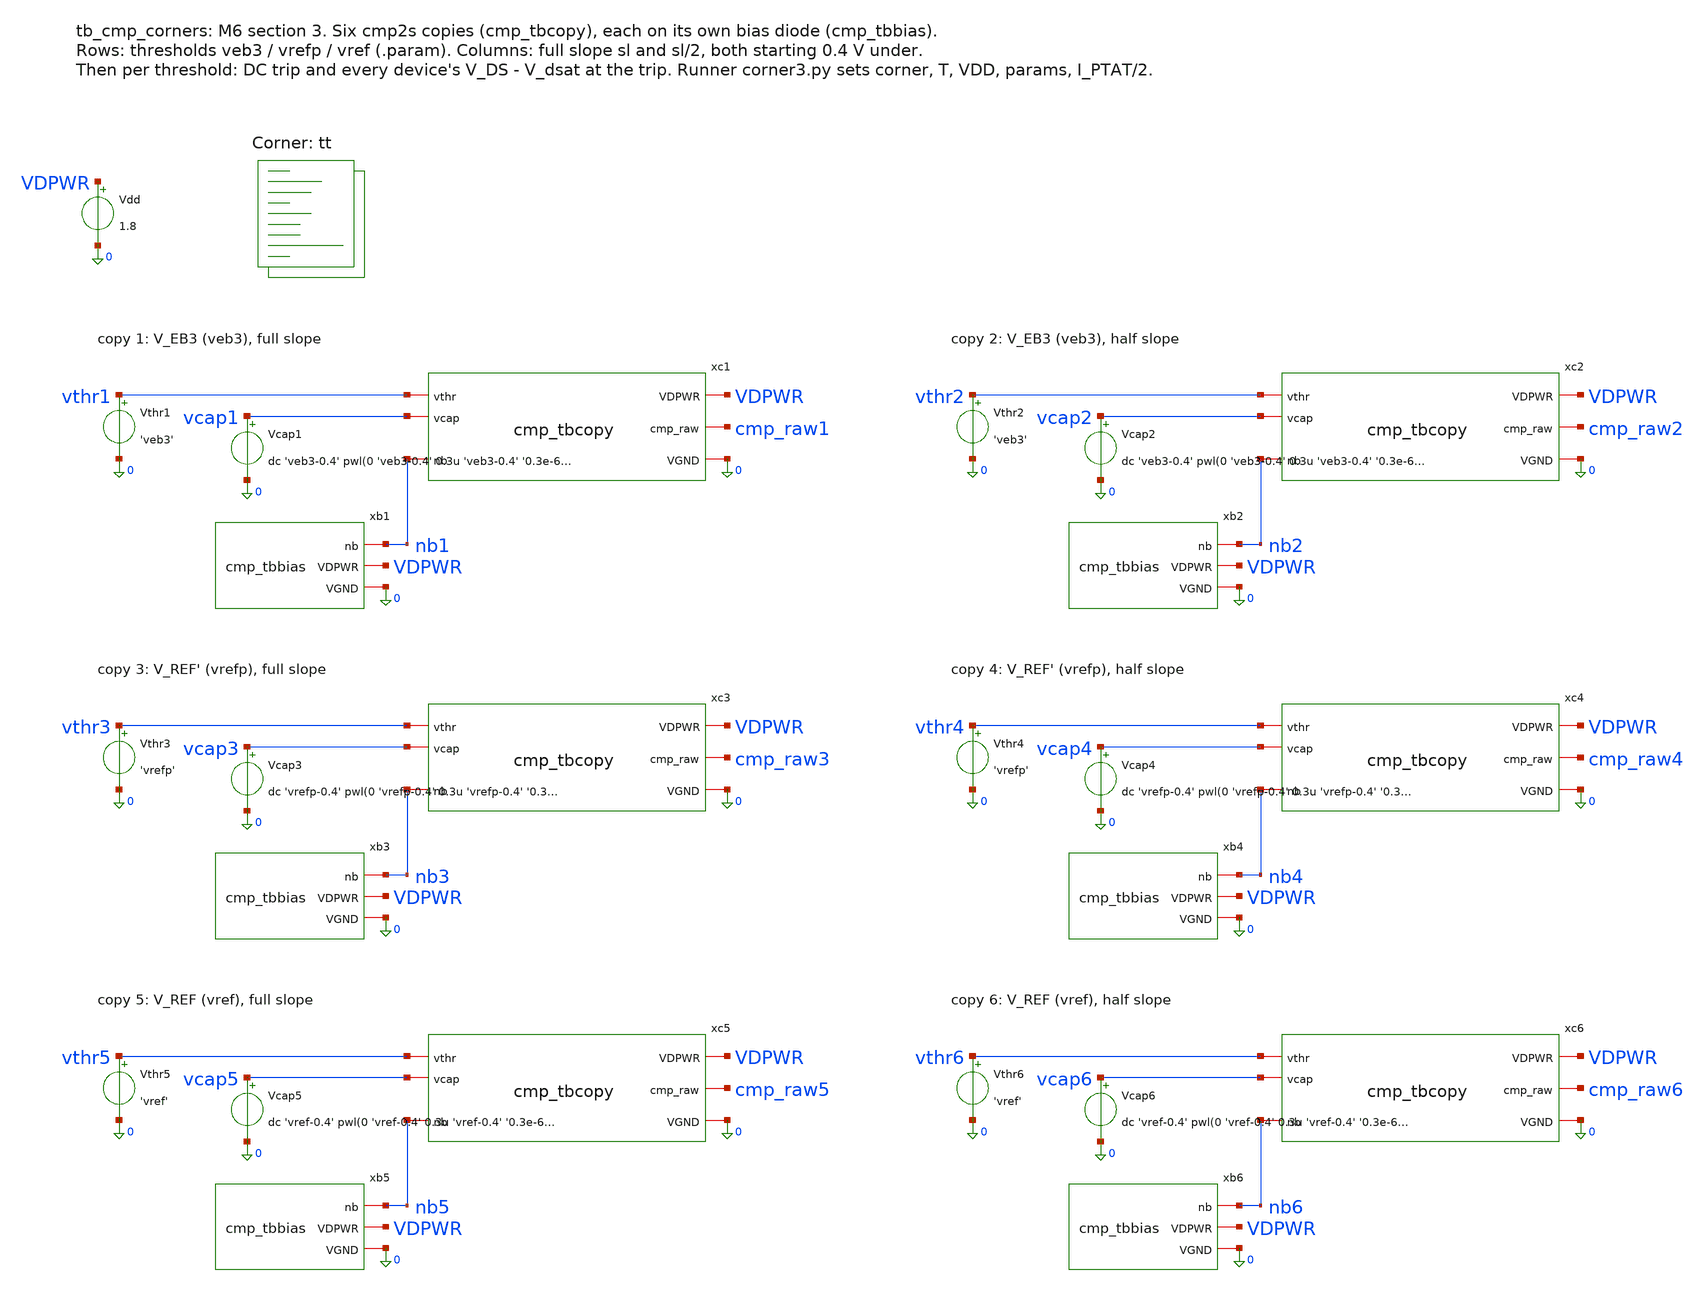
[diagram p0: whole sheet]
** sch_path: xschem/tb_cmp_corners.sch
**.subckt tb_cmp_corners
xc1 vthr1 vcap1 nb1 VDPWR cmp_raw1 0 cmp_tbcopy
xb1 nb1 VDPWR 0 cmp_tbbias
Vthr1 vthr1 0 'veb3'
Vcap1 vcap1 0 dc 'veb3-0.4' pwl(0 'veb3-0.4' 0.3u 'veb3-0.4' '0.3e-6+0.46/sl' 'veb3+0.06')
xc2 vthr2 vcap2 nb2 VDPWR cmp_raw2 0 cmp_tbcopy
xb2 nb2 VDPWR 0 cmp_tbbias
Vthr2 vthr2 0 'veb3'
Vcap2 vcap2 0 dc 'veb3-0.4' pwl(0 'veb3-0.4' 0.3u 'veb3-0.4' '0.3e-6+0.92/sl' 'veb3+0.06')
xc3 vthr3 vcap3 nb3 VDPWR cmp_raw3 0 cmp_tbcopy
xb3 nb3 VDPWR 0 cmp_tbbias
Vthr3 vthr3 0 'vrefp'
Vcap3 vcap3 0 dc 'vrefp-0.4' pwl(0 'vrefp-0.4' 0.3u 'vrefp-0.4' '0.3e-6+0.46/sl' 'vrefp+0.06')
xc4 vthr4 vcap4 nb4 VDPWR cmp_raw4 0 cmp_tbcopy
xb4 nb4 VDPWR 0 cmp_tbbias
Vthr4 vthr4 0 'vrefp'
Vcap4 vcap4 0 dc 'vrefp-0.4' pwl(0 'vrefp-0.4' 0.3u 'vrefp-0.4' '0.3e-6+0.92/sl' 'vrefp+0.06')
xc5 vthr5 vcap5 nb5 VDPWR cmp_raw5 0 cmp_tbcopy
xb5 nb5 VDPWR 0 cmp_tbbias
Vthr5 vthr5 0 'vref'
Vcap5 vcap5 0 dc 'vref-0.4' pwl(0 'vref-0.4' 0.3u 'vref-0.4' '0.3e-6+0.46/sl' 'vref+0.06')
xc6 vthr6 vcap6 nb6 VDPWR cmp_raw6 0 cmp_tbcopy
xb6 nb6 VDPWR 0 cmp_tbbias
Vthr6 vthr6 0 'vref'
Vcap6 vcap6 0 dc 'vref-0.4' pwl(0 'vref-0.4' 0.3u 'vref-0.4' '0.3e-6+0.92/sl' 'vref+0.06')
Vdd VDPWR 0 1.8
**** begin user architecture code

.param vref=1.2432 veb3=0.7096 vrefp=0.9605 sl=0.274e6
.include /foss/pdks/sky130A/libs.ref/sky130_fd_sc_hd/spice/sky130_fd_sc_hd.spice
.option method=gear
.temp 25
.control
save all @m.xc1.x1.xm1a.msky130_fd_pr__nfet_01v8_lvt[vds]
+ @m.xc1.x1.xm1a.msky130_fd_pr__nfet_01v8_lvt[vdsat] @m.xc1.x1.xm1b.msky130_fd_pr__nfet_01v8_lvt[vds] @m.xc1.x1.xm1b.msky130_fd_pr__nfet_01v8_lvt[vdsat]
+ @m.xc1.x1.xm2b.msky130_fd_pr__pfet_01v8_lvt[vds] @m.xc1.x1.xm2b.msky130_fd_pr__pfet_01v8_lvt[vdsat] @m.xc1.x1.xm3.msky130_fd_pr__pfet_01v8_lvt[vds]
+ @m.xc1.x1.xm3.msky130_fd_pr__pfet_01v8_lvt[vdsat] @m.xc1.xmnb3.msky130_fd_pr__nfet_01v8[vds] @m.xc1.xmnb3.msky130_fd_pr__nfet_01v8[vdsat]
+ @m.xc2.x1.xm1a.msky130_fd_pr__nfet_01v8_lvt[vds] @m.xc2.x1.xm1a.msky130_fd_pr__nfet_01v8_lvt[vdsat] @m.xc2.x1.xm1b.msky130_fd_pr__nfet_01v8_lvt[vds]
+ @m.xc2.x1.xm1b.msky130_fd_pr__nfet_01v8_lvt[vdsat] @m.xc2.x1.xm2b.msky130_fd_pr__pfet_01v8_lvt[vds] @m.xc2.x1.xm2b.msky130_fd_pr__pfet_01v8_lvt[vdsat]
+ @m.xc2.x1.xm3.msky130_fd_pr__pfet_01v8_lvt[vds] @m.xc2.x1.xm3.msky130_fd_pr__pfet_01v8_lvt[vdsat] @m.xc2.xmnb3.msky130_fd_pr__nfet_01v8[vds]
+ @m.xc2.xmnb3.msky130_fd_pr__nfet_01v8[vdsat] @m.xc3.x1.xm1a.msky130_fd_pr__nfet_01v8_lvt[vds] @m.xc3.x1.xm1a.msky130_fd_pr__nfet_01v8_lvt[vdsat]
+ @m.xc3.x1.xm1b.msky130_fd_pr__nfet_01v8_lvt[vds] @m.xc3.x1.xm1b.msky130_fd_pr__nfet_01v8_lvt[vdsat] @m.xc3.x1.xm2b.msky130_fd_pr__pfet_01v8_lvt[vds]
+ @m.xc3.x1.xm2b.msky130_fd_pr__pfet_01v8_lvt[vdsat] @m.xc3.x1.xm3.msky130_fd_pr__pfet_01v8_lvt[vds] @m.xc3.x1.xm3.msky130_fd_pr__pfet_01v8_lvt[vdsat]
+ @m.xc3.xmnb3.msky130_fd_pr__nfet_01v8[vds] @m.xc3.xmnb3.msky130_fd_pr__nfet_01v8[vdsat] @m.xc4.x1.xm1a.msky130_fd_pr__nfet_01v8_lvt[vds]
+ @m.xc4.x1.xm1a.msky130_fd_pr__nfet_01v8_lvt[vdsat] @m.xc4.x1.xm1b.msky130_fd_pr__nfet_01v8_lvt[vds] @m.xc4.x1.xm1b.msky130_fd_pr__nfet_01v8_lvt[vdsat]
+ @m.xc4.x1.xm2b.msky130_fd_pr__pfet_01v8_lvt[vds] @m.xc4.x1.xm2b.msky130_fd_pr__pfet_01v8_lvt[vdsat] @m.xc4.x1.xm3.msky130_fd_pr__pfet_01v8_lvt[vds]
+ @m.xc4.x1.xm3.msky130_fd_pr__pfet_01v8_lvt[vdsat] @m.xc4.xmnb3.msky130_fd_pr__nfet_01v8[vds] @m.xc4.xmnb3.msky130_fd_pr__nfet_01v8[vdsat]
+ @m.xc5.x1.xm1a.msky130_fd_pr__nfet_01v8_lvt[vds] @m.xc5.x1.xm1a.msky130_fd_pr__nfet_01v8_lvt[vdsat] @m.xc5.x1.xm1b.msky130_fd_pr__nfet_01v8_lvt[vds]
+ @m.xc5.x1.xm1b.msky130_fd_pr__nfet_01v8_lvt[vdsat] @m.xc5.x1.xm2b.msky130_fd_pr__pfet_01v8_lvt[vds] @m.xc5.x1.xm2b.msky130_fd_pr__pfet_01v8_lvt[vdsat]
+ @m.xc5.x1.xm3.msky130_fd_pr__pfet_01v8_lvt[vds] @m.xc5.x1.xm3.msky130_fd_pr__pfet_01v8_lvt[vdsat] @m.xc5.xmnb3.msky130_fd_pr__nfet_01v8[vds]
+ @m.xc5.xmnb3.msky130_fd_pr__nfet_01v8[vdsat] @m.xc6.x1.xm1a.msky130_fd_pr__nfet_01v8_lvt[vds] @m.xc6.x1.xm1a.msky130_fd_pr__nfet_01v8_lvt[vdsat]
+ @m.xc6.x1.xm1b.msky130_fd_pr__nfet_01v8_lvt[vds] @m.xc6.x1.xm1b.msky130_fd_pr__nfet_01v8_lvt[vdsat] @m.xc6.x1.xm2b.msky130_fd_pr__pfet_01v8_lvt[vds]
+ @m.xc6.x1.xm2b.msky130_fd_pr__pfet_01v8_lvt[vdsat] @m.xc6.x1.xm3.msky130_fd_pr__pfet_01v8_lvt[vds] @m.xc6.x1.xm3.msky130_fd_pr__pfet_01v8_lvt[vdsat]
+ @m.xc6.xmnb3.msky130_fd_pr__nfet_01v8[vds] @m.xc6.xmnb3.msky130_fd_pr__nfet_01v8[vdsat]
tran 0.2n 3.85u 0 0.2n
meas tran to1 when v(cmp_raw1)=0.9 rise=1
meas tran to2 when v(cmp_raw2)=0.9 rise=1
meas tran to3 when v(cmp_raw3)=0.9 rise=1
meas tran to4 when v(cmp_raw4)=0.9 rise=1
meas tran to5 when v(cmp_raw5)=0.9 rise=1
meas tran to6 when v(cmp_raw6)=0.9 rise=1
echo RESULT to1=$&to1 to2=$&to2 to3=$&to3 to4=$&to4 to5=$&to5 to6=$&to6
* V_DS - V_dsat (mV) of the key devices at the moment n2 crosses 0.9 V on the ramp
meas tran tf1 when v(xc1.ib_cmp2)=0.9 rise=1
let gm1a_1 = (abs(@m.xc1.x1.xm1a.msky130_fd_pr__nfet_01v8_lvt[vds]) -
+ abs(@m.xc1.x1.xm1a.msky130_fd_pr__nfet_01v8_lvt[vdsat]))*1e3
meas tran fm1a_1 find gm1a_1 at=$&tf1
let gm1b_1 = (abs(@m.xc1.x1.xm1b.msky130_fd_pr__nfet_01v8_lvt[vds]) -
+ abs(@m.xc1.x1.xm1b.msky130_fd_pr__nfet_01v8_lvt[vdsat]))*1e3
meas tran fm1b_1 find gm1b_1 at=$&tf1
let gm2b_1 = (abs(@m.xc1.x1.xm2b.msky130_fd_pr__pfet_01v8_lvt[vds]) -
+ abs(@m.xc1.x1.xm2b.msky130_fd_pr__pfet_01v8_lvt[vdsat]))*1e3
meas tran fm2b_1 find gm2b_1 at=$&tf1
let gm3_1 = (abs(@m.xc1.x1.xm3.msky130_fd_pr__pfet_01v8_lvt[vds]) -
+ abs(@m.xc1.x1.xm3.msky130_fd_pr__pfet_01v8_lvt[vdsat]))*1e3
meas tran fm3_1 find gm3_1 at=$&tf1
let gmnb3_1 = (abs(@m.xc1.xmnb3.msky130_fd_pr__nfet_01v8[vds]) -
+ abs(@m.xc1.xmnb3.msky130_fd_pr__nfet_01v8[vdsat]))*1e3
meas tran fmnb3_1 find gmnb3_1 at=$&tf1
meas tran fn1_1 find v(xc1.x1.n1) at=$&tf1
meas tran ftl_1 find v(xc1.ib_cmp1) at=$&tf1
echo FLIP k=1 m1a=$&fm1a_1 m1b=$&fm1b_1 m2b=$&fm2b_1 m3=$&fm3_1 mnb3=$&fmnb3_1 n1=$&fn1_1
+ tail=$&ftl_1
meas tran tf2 when v(xc2.ib_cmp2)=0.9 rise=1
let gm1a_2 = (abs(@m.xc2.x1.xm1a.msky130_fd_pr__nfet_01v8_lvt[vds]) -
+ abs(@m.xc2.x1.xm1a.msky130_fd_pr__nfet_01v8_lvt[vdsat]))*1e3
meas tran fm1a_2 find gm1a_2 at=$&tf2
let gm1b_2 = (abs(@m.xc2.x1.xm1b.msky130_fd_pr__nfet_01v8_lvt[vds]) -
+ abs(@m.xc2.x1.xm1b.msky130_fd_pr__nfet_01v8_lvt[vdsat]))*1e3
meas tran fm1b_2 find gm1b_2 at=$&tf2
let gm2b_2 = (abs(@m.xc2.x1.xm2b.msky130_fd_pr__pfet_01v8_lvt[vds]) -
+ abs(@m.xc2.x1.xm2b.msky130_fd_pr__pfet_01v8_lvt[vdsat]))*1e3
meas tran fm2b_2 find gm2b_2 at=$&tf2
let gm3_2 = (abs(@m.xc2.x1.xm3.msky130_fd_pr__pfet_01v8_lvt[vds]) -
+ abs(@m.xc2.x1.xm3.msky130_fd_pr__pfet_01v8_lvt[vdsat]))*1e3
meas tran fm3_2 find gm3_2 at=$&tf2
let gmnb3_2 = (abs(@m.xc2.xmnb3.msky130_fd_pr__nfet_01v8[vds]) -
+ abs(@m.xc2.xmnb3.msky130_fd_pr__nfet_01v8[vdsat]))*1e3
meas tran fmnb3_2 find gmnb3_2 at=$&tf2
meas tran fn1_2 find v(xc2.x1.n1) at=$&tf2
meas tran ftl_2 find v(xc2.ib_cmp1) at=$&tf2
echo FLIP k=2 m1a=$&fm1a_2 m1b=$&fm1b_2 m2b=$&fm2b_2 m3=$&fm3_2 mnb3=$&fmnb3_2 n1=$&fn1_2
+ tail=$&ftl_2
meas tran tf3 when v(xc3.ib_cmp2)=0.9 rise=1
let gm1a_3 = (abs(@m.xc3.x1.xm1a.msky130_fd_pr__nfet_01v8_lvt[vds]) -
+ abs(@m.xc3.x1.xm1a.msky130_fd_pr__nfet_01v8_lvt[vdsat]))*1e3
meas tran fm1a_3 find gm1a_3 at=$&tf3
let gm1b_3 = (abs(@m.xc3.x1.xm1b.msky130_fd_pr__nfet_01v8_lvt[vds]) -
+ abs(@m.xc3.x1.xm1b.msky130_fd_pr__nfet_01v8_lvt[vdsat]))*1e3
meas tran fm1b_3 find gm1b_3 at=$&tf3
let gm2b_3 = (abs(@m.xc3.x1.xm2b.msky130_fd_pr__pfet_01v8_lvt[vds]) -
+ abs(@m.xc3.x1.xm2b.msky130_fd_pr__pfet_01v8_lvt[vdsat]))*1e3
meas tran fm2b_3 find gm2b_3 at=$&tf3
let gm3_3 = (abs(@m.xc3.x1.xm3.msky130_fd_pr__pfet_01v8_lvt[vds]) -
+ abs(@m.xc3.x1.xm3.msky130_fd_pr__pfet_01v8_lvt[vdsat]))*1e3
meas tran fm3_3 find gm3_3 at=$&tf3
let gmnb3_3 = (abs(@m.xc3.xmnb3.msky130_fd_pr__nfet_01v8[vds]) -
+ abs(@m.xc3.xmnb3.msky130_fd_pr__nfet_01v8[vdsat]))*1e3
meas tran fmnb3_3 find gmnb3_3 at=$&tf3
meas tran fn1_3 find v(xc3.x1.n1) at=$&tf3
meas tran ftl_3 find v(xc3.ib_cmp1) at=$&tf3
echo FLIP k=3 m1a=$&fm1a_3 m1b=$&fm1b_3 m2b=$&fm2b_3 m3=$&fm3_3 mnb3=$&fmnb3_3 n1=$&fn1_3
+ tail=$&ftl_3
meas tran tf4 when v(xc4.ib_cmp2)=0.9 rise=1
let gm1a_4 = (abs(@m.xc4.x1.xm1a.msky130_fd_pr__nfet_01v8_lvt[vds]) -
+ abs(@m.xc4.x1.xm1a.msky130_fd_pr__nfet_01v8_lvt[vdsat]))*1e3
meas tran fm1a_4 find gm1a_4 at=$&tf4
let gm1b_4 = (abs(@m.xc4.x1.xm1b.msky130_fd_pr__nfet_01v8_lvt[vds]) -
+ abs(@m.xc4.x1.xm1b.msky130_fd_pr__nfet_01v8_lvt[vdsat]))*1e3
meas tran fm1b_4 find gm1b_4 at=$&tf4
let gm2b_4 = (abs(@m.xc4.x1.xm2b.msky130_fd_pr__pfet_01v8_lvt[vds]) -
+ abs(@m.xc4.x1.xm2b.msky130_fd_pr__pfet_01v8_lvt[vdsat]))*1e3
meas tran fm2b_4 find gm2b_4 at=$&tf4
let gm3_4 = (abs(@m.xc4.x1.xm3.msky130_fd_pr__pfet_01v8_lvt[vds]) -
+ abs(@m.xc4.x1.xm3.msky130_fd_pr__pfet_01v8_lvt[vdsat]))*1e3
meas tran fm3_4 find gm3_4 at=$&tf4
let gmnb3_4 = (abs(@m.xc4.xmnb3.msky130_fd_pr__nfet_01v8[vds]) -
+ abs(@m.xc4.xmnb3.msky130_fd_pr__nfet_01v8[vdsat]))*1e3
meas tran fmnb3_4 find gmnb3_4 at=$&tf4
meas tran fn1_4 find v(xc4.x1.n1) at=$&tf4
meas tran ftl_4 find v(xc4.ib_cmp1) at=$&tf4
echo FLIP k=4 m1a=$&fm1a_4 m1b=$&fm1b_4 m2b=$&fm2b_4 m3=$&fm3_4 mnb3=$&fmnb3_4 n1=$&fn1_4
+ tail=$&ftl_4
meas tran tf5 when v(xc5.ib_cmp2)=0.9 rise=1
let gm1a_5 = (abs(@m.xc5.x1.xm1a.msky130_fd_pr__nfet_01v8_lvt[vds]) -
+ abs(@m.xc5.x1.xm1a.msky130_fd_pr__nfet_01v8_lvt[vdsat]))*1e3
meas tran fm1a_5 find gm1a_5 at=$&tf5
let gm1b_5 = (abs(@m.xc5.x1.xm1b.msky130_fd_pr__nfet_01v8_lvt[vds]) -
+ abs(@m.xc5.x1.xm1b.msky130_fd_pr__nfet_01v8_lvt[vdsat]))*1e3
meas tran fm1b_5 find gm1b_5 at=$&tf5
let gm2b_5 = (abs(@m.xc5.x1.xm2b.msky130_fd_pr__pfet_01v8_lvt[vds]) -
+ abs(@m.xc5.x1.xm2b.msky130_fd_pr__pfet_01v8_lvt[vdsat]))*1e3
meas tran fm2b_5 find gm2b_5 at=$&tf5
let gm3_5 = (abs(@m.xc5.x1.xm3.msky130_fd_pr__pfet_01v8_lvt[vds]) -
+ abs(@m.xc5.x1.xm3.msky130_fd_pr__pfet_01v8_lvt[vdsat]))*1e3
meas tran fm3_5 find gm3_5 at=$&tf5
let gmnb3_5 = (abs(@m.xc5.xmnb3.msky130_fd_pr__nfet_01v8[vds]) -
+ abs(@m.xc5.xmnb3.msky130_fd_pr__nfet_01v8[vdsat]))*1e3
meas tran fmnb3_5 find gmnb3_5 at=$&tf5
meas tran fn1_5 find v(xc5.x1.n1) at=$&tf5
meas tran ftl_5 find v(xc5.ib_cmp1) at=$&tf5
echo FLIP k=5 m1a=$&fm1a_5 m1b=$&fm1b_5 m2b=$&fm2b_5 m3=$&fm3_5 mnb3=$&fmnb3_5 n1=$&fn1_5
+ tail=$&ftl_5
meas tran tf6 when v(xc6.ib_cmp2)=0.9 rise=1
let gm1a_6 = (abs(@m.xc6.x1.xm1a.msky130_fd_pr__nfet_01v8_lvt[vds]) -
+ abs(@m.xc6.x1.xm1a.msky130_fd_pr__nfet_01v8_lvt[vdsat]))*1e3
meas tran fm1a_6 find gm1a_6 at=$&tf6
let gm1b_6 = (abs(@m.xc6.x1.xm1b.msky130_fd_pr__nfet_01v8_lvt[vds]) -
+ abs(@m.xc6.x1.xm1b.msky130_fd_pr__nfet_01v8_lvt[vdsat]))*1e3
meas tran fm1b_6 find gm1b_6 at=$&tf6
let gm2b_6 = (abs(@m.xc6.x1.xm2b.msky130_fd_pr__pfet_01v8_lvt[vds]) -
+ abs(@m.xc6.x1.xm2b.msky130_fd_pr__pfet_01v8_lvt[vdsat]))*1e3
meas tran fm2b_6 find gm2b_6 at=$&tf6
let gm3_6 = (abs(@m.xc6.x1.xm3.msky130_fd_pr__pfet_01v8_lvt[vds]) -
+ abs(@m.xc6.x1.xm3.msky130_fd_pr__pfet_01v8_lvt[vdsat]))*1e3
meas tran fm3_6 find gm3_6 at=$&tf6
let gmnb3_6 = (abs(@m.xc6.xmnb3.msky130_fd_pr__nfet_01v8[vds]) -
+ abs(@m.xc6.xmnb3.msky130_fd_pr__nfet_01v8[vdsat]))*1e3
meas tran fmnb3_6 find gmnb3_6 at=$&tf6
meas tran fn1_6 find v(xc6.x1.n1) at=$&tf6
meas tran ftl_6 find v(xc6.ib_cmp1) at=$&tf6
echo FLIP k=6 m1a=$&fm1a_6 m1b=$&fm1b_6 m2b=$&fm2b_6 m3=$&fm3_6 mnb3=$&fmnb3_6 n1=$&fn1_6
+ tail=$&ftl_6
* per threshold: static trip (DC sweep, 5 uV steps), then V_DS - V_dsat (mV) of every device at that
*+ trip
dc vcap1 0.7046 0.7146 5u
meas dc trip1 when v(cmp_raw1)=0.9 rise=1
echo RESULT trip1=$&trip1
alter @vcap1[dc] = $&trip1
op
let m1a_1 = (abs(@m.xc1.x1.xm1a.msky130_fd_pr__nfet_01v8_lvt[vds]) -
+ abs(@m.xc1.x1.xm1a.msky130_fd_pr__nfet_01v8_lvt[vdsat]))*1e3
let m1b_1 = (abs(@m.xc1.x1.xm1b.msky130_fd_pr__nfet_01v8_lvt[vds]) -
+ abs(@m.xc1.x1.xm1b.msky130_fd_pr__nfet_01v8_lvt[vdsat]))*1e3
let m2a_1 = (abs(@m.xc1.x1.xm2a.msky130_fd_pr__pfet_01v8_lvt[vds]) -
+ abs(@m.xc1.x1.xm2a.msky130_fd_pr__pfet_01v8_lvt[vdsat]))*1e3
let m2b_1 = (abs(@m.xc1.x1.xm2b.msky130_fd_pr__pfet_01v8_lvt[vds]) -
+ abs(@m.xc1.x1.xm2b.msky130_fd_pr__pfet_01v8_lvt[vdsat]))*1e3
let m3_1 = (abs(@m.xc1.x1.xm3.msky130_fd_pr__pfet_01v8_lvt[vds]) -
+ abs(@m.xc1.x1.xm3.msky130_fd_pr__pfet_01v8_lvt[vdsat]))*1e3
let mnb3_1 = (abs(@m.xc1.xmnb3.msky130_fd_pr__nfet_01v8[vds]) -
+ abs(@m.xc1.xmnb3.msky130_fd_pr__nfet_01v8[vdsat]))*1e3
let mnb4_1 = (abs(@m.xc1.xmnb4.msky130_fd_pr__nfet_01v8[vds]) -
+ abs(@m.xc1.xmnb4.msky130_fd_pr__nfet_01v8[vdsat]))*1e3
let n1_1 = v(xc1.x1.n1)
let tl_1 = v(xc1.ib_cmp1)
let nd_1 = v(xc1.x1.nd)
echo MARGIN k=1 m1a=$&m1a_1 m1b=$&m1b_1 m2a=$&m2a_1 m2b=$&m2b_1 m3=$&m3_1 mnb3=$&mnb3_1
+ mnb4=$&mnb4_1 n1=$&n1_1 tail=$&tl_1 nd=$&nd_1
dc vcap3 0.9555 0.9655 5u
meas dc trip3 when v(cmp_raw3)=0.9 rise=1
echo RESULT trip3=$&trip3
alter @vcap3[dc] = $&trip3
op
let m1a_3 = (abs(@m.xc3.x1.xm1a.msky130_fd_pr__nfet_01v8_lvt[vds]) -
+ abs(@m.xc3.x1.xm1a.msky130_fd_pr__nfet_01v8_lvt[vdsat]))*1e3
let m1b_3 = (abs(@m.xc3.x1.xm1b.msky130_fd_pr__nfet_01v8_lvt[vds]) -
+ abs(@m.xc3.x1.xm1b.msky130_fd_pr__nfet_01v8_lvt[vdsat]))*1e3
let m2a_3 = (abs(@m.xc3.x1.xm2a.msky130_fd_pr__pfet_01v8_lvt[vds]) -
+ abs(@m.xc3.x1.xm2a.msky130_fd_pr__pfet_01v8_lvt[vdsat]))*1e3
let m2b_3 = (abs(@m.xc3.x1.xm2b.msky130_fd_pr__pfet_01v8_lvt[vds]) -
+ abs(@m.xc3.x1.xm2b.msky130_fd_pr__pfet_01v8_lvt[vdsat]))*1e3
let m3_3 = (abs(@m.xc3.x1.xm3.msky130_fd_pr__pfet_01v8_lvt[vds]) -
+ abs(@m.xc3.x1.xm3.msky130_fd_pr__pfet_01v8_lvt[vdsat]))*1e3
let mnb3_3 = (abs(@m.xc3.xmnb3.msky130_fd_pr__nfet_01v8[vds]) -
+ abs(@m.xc3.xmnb3.msky130_fd_pr__nfet_01v8[vdsat]))*1e3
let mnb4_3 = (abs(@m.xc3.xmnb4.msky130_fd_pr__nfet_01v8[vds]) -
+ abs(@m.xc3.xmnb4.msky130_fd_pr__nfet_01v8[vdsat]))*1e3
let n1_3 = v(xc3.x1.n1)
let tl_3 = v(xc3.ib_cmp1)
let nd_3 = v(xc3.x1.nd)
echo MARGIN k=3 m1a=$&m1a_3 m1b=$&m1b_3 m2a=$&m2a_3 m2b=$&m2b_3 m3=$&m3_3 mnb3=$&mnb3_3
+ mnb4=$&mnb4_3 n1=$&n1_3 tail=$&tl_3 nd=$&nd_3
dc vcap5 1.2382 1.2482 5u
meas dc trip5 when v(cmp_raw5)=0.9 rise=1
echo RESULT trip5=$&trip5
alter @vcap5[dc] = $&trip5
op
let m1a_5 = (abs(@m.xc5.x1.xm1a.msky130_fd_pr__nfet_01v8_lvt[vds]) -
+ abs(@m.xc5.x1.xm1a.msky130_fd_pr__nfet_01v8_lvt[vdsat]))*1e3
let m1b_5 = (abs(@m.xc5.x1.xm1b.msky130_fd_pr__nfet_01v8_lvt[vds]) -
+ abs(@m.xc5.x1.xm1b.msky130_fd_pr__nfet_01v8_lvt[vdsat]))*1e3
let m2a_5 = (abs(@m.xc5.x1.xm2a.msky130_fd_pr__pfet_01v8_lvt[vds]) -
+ abs(@m.xc5.x1.xm2a.msky130_fd_pr__pfet_01v8_lvt[vdsat]))*1e3
let m2b_5 = (abs(@m.xc5.x1.xm2b.msky130_fd_pr__pfet_01v8_lvt[vds]) -
+ abs(@m.xc5.x1.xm2b.msky130_fd_pr__pfet_01v8_lvt[vdsat]))*1e3
let m3_5 = (abs(@m.xc5.x1.xm3.msky130_fd_pr__pfet_01v8_lvt[vds]) -
+ abs(@m.xc5.x1.xm3.msky130_fd_pr__pfet_01v8_lvt[vdsat]))*1e3
let mnb3_5 = (abs(@m.xc5.xmnb3.msky130_fd_pr__nfet_01v8[vds]) -
+ abs(@m.xc5.xmnb3.msky130_fd_pr__nfet_01v8[vdsat]))*1e3
let mnb4_5 = (abs(@m.xc5.xmnb4.msky130_fd_pr__nfet_01v8[vds]) -
+ abs(@m.xc5.xmnb4.msky130_fd_pr__nfet_01v8[vdsat]))*1e3
let n1_5 = v(xc5.x1.n1)
let tl_5 = v(xc5.ib_cmp1)
let nd_5 = v(xc5.x1.nd)
echo MARGIN k=5 m1a=$&m1a_5 m1b=$&m1b_5 m2a=$&m2a_5 m2b=$&m2b_5 m3=$&m3_5 mnb3=$&mnb3_5
+ mnb4=$&mnb4_5 n1=$&n1_5 tail=$&tl_5 nd=$&nd_5
.endc

.lib $::SKYWATER_MODELS/sky130.lib.spice tt
**** end user architecture code
**.ends

* expanding   symbol:  cmp_tbcopy.sym # of pins=6
** sym_path: xschem/cmp_tbcopy.sym
** sch_path: xschem/cmp_tbcopy.sch
.subckt cmp_tbcopy vthr vcap nb VDPWR cmp_raw VGND
*.ipin vthr
*.ipin vcap
*.iopin nb
*.iopin VDPWR
*.opin cmp_raw
*.iopin VGND
x1 vthr vcap ib_cmp1 ib_cmp2 VDPWR cmp_raw VGND cmp2s
XMNB3 ib_cmp1 nb VGND VGND sky130_fd_pr__nfet_01v8 L=8 W=4 nf=1 ad='int((1 + 1)/2) * 4 / 1 * 0.29' as='int((1 + 2)/2) * 4 / 1 * 0.29'
+ pd='2*int((1 + 1)/2) * (4 / 1 + 0.29)' ps='2*int((1 + 2)/2) * (4 / 1 + 0.29)' nrd='0.29 / 4 ' nrs='0.29 / 4 '
+ sa=0 sb=0 sd=0 mult=4 m=4
XMNB4 ib_cmp2 nb VGND VGND sky130_fd_pr__nfet_01v8 L=8 W=4 nf=1 ad='int((1 + 1)/2) * 4 / 1 * 0.29' as='int((1 + 2)/2) * 4 / 1 * 0.29'
+ pd='2*int((1 + 1)/2) * (4 / 1 + 0.29)' ps='2*int((1 + 2)/2) * (4 / 1 + 0.29)' nrd='0.29 / 4 ' nrs='0.29 / 4 '
+ sa=0 sb=0 sd=0 mult=4 m=4
Cw1 ib_cmp1 VGND 40f m=1
Cw2 ib_cmp2 VGND 40f m=1
.ends


* expanding   symbol:  cmp_tbbias.sym # of pins=3
** sym_path: xschem/cmp_tbbias.sym
** sch_path: xschem/cmp_tbbias.sch
.subckt cmp_tbbias nb VDPWR VGND
*.iopin VDPWR
*.iopin nb
*.iopin VGND
Iref VDPWR nb 1.386u
XMNB1 nb nb VGND VGND sky130_fd_pr__nfet_01v8 L=8 W=4 nf=1 ad='int((1 + 1)/2) * 4 / 1 * 0.29' as='int((1 + 2)/2) * 4 / 1 * 0.29'
+ pd='2*int((1 + 1)/2) * (4 / 1 + 0.29)' ps='2*int((1 + 2)/2) * (4 / 1 + 0.29)' nrd='0.29 / 4 ' nrs='0.29 / 4 '
+ sa=0 sb=0 sd=0 mult=1 m=1
.ends


* expanding   symbol:  cmp2s.sym # of pins=7
** sym_path: xschem/cmp2s.sym
** sch_path: xschem/cmp2s.sch
.subckt cmp2s vthr vcap ib_cmp1 ib_cmp2 VDPWR cmp_raw VGND
*.iopin VDPWR
*.iopin VGND
*.ipin vthr
*.ipin vcap
*.iopin ib_cmp1
*.iopin ib_cmp2
*.opin cmp_raw
XM2a nd nd VDPWR VDPWR sky130_fd_pr__pfet_01v8_lvt L=4 W=4 nf=1 ad='int((1 + 1)/2) * 4 / 1 * 0.29' as='int((1 + 2)/2) * 4 / 1 * 0.29'
+ pd='2*int((1 + 1)/2) * (4 / 1 + 0.29)' ps='2*int((1 + 2)/2) * (4 / 1 + 0.29)' nrd='0.29 / 4 ' nrs='0.29 / 4 '
+ sa=0 sb=0 sd=0 mult=8 m=8
XM2b n1 nd VDPWR VDPWR sky130_fd_pr__pfet_01v8_lvt L=4 W=4 nf=1 ad='int((1 + 1)/2) * 4 / 1 * 0.29' as='int((1 + 2)/2) * 4 / 1 * 0.29'
+ pd='2*int((1 + 1)/2) * (4 / 1 + 0.29)' ps='2*int((1 + 2)/2) * (4 / 1 + 0.29)' nrd='0.29 / 4 ' nrs='0.29 / 4 '
+ sa=0 sb=0 sd=0 mult=8 m=8
XM1a nd vthr ib_cmp1 VGND sky130_fd_pr__nfet_01v8_lvt L=1.75 W=10 nf=1 ad='int((1 + 1)/2) * 10 / 1 * 0.29'
+ as='int((1 + 2)/2) * 10 / 1 * 0.29' pd='2*int((1 + 1)/2) * (10 / 1 + 0.29)' ps='2*int((1 + 2)/2) * (10 / 1 + 0.29)'
+ nrd='0.29 / 10 ' nrs='0.29 / 10 ' sa=0 sb=0 sd=0 mult=6 m=6
XM1b n1 vcap ib_cmp1 VGND sky130_fd_pr__nfet_01v8_lvt L=1.75 W=10 nf=1 ad='int((1 + 1)/2) * 10 / 1 * 0.29'
+ as='int((1 + 2)/2) * 10 / 1 * 0.29' pd='2*int((1 + 1)/2) * (10 / 1 + 0.29)' ps='2*int((1 + 2)/2) * (10 / 1 + 0.29)'
+ nrd='0.29 / 10 ' nrs='0.29 / 10 ' sa=0 sb=0 sd=0 mult=6 m=6
XM3 ib_cmp2 n1 VDPWR VDPWR sky130_fd_pr__pfet_01v8_lvt L=1 W=4 nf=1 ad='int((1 + 1)/2) * 4 / 1 * 0.29'
+ as='int((1 + 2)/2) * 4 / 1 * 0.29' pd='2*int((1 + 1)/2) * (4 / 1 + 0.29)' ps='2*int((1 + 2)/2) * (4 / 1 + 0.29)'
+ nrd='0.29 / 4 ' nrs='0.29 / 4 ' sa=0 sb=0 sd=0 mult=3 m=3
XMIP x ib_cmp2 VDPWR VDPWR sky130_fd_pr__pfet_01v8 L=1 W=0.42 nf=1 ad='int((1 + 1)/2) * 0.42 / 1 * 0.29'
+ as='int((1 + 2)/2) * 0.42 / 1 * 0.29' pd='2*int((1 + 1)/2) * (0.42 / 1 + 0.29)' ps='2*int((1 + 2)/2) * (0.42 / 1 + 0.29)'
+ nrd='0.29 / 0.42 ' nrs='0.29 / 0.42 ' sa=0 sb=0 sd=0 mult=1 m=1
XMIN x ib_cmp2 VGND VGND sky130_fd_pr__nfet_01v8 L=0.15 W=2 nf=1 ad='int((1 + 1)/2) * 2 / 1 * 0.29' as='int((1 + 2)/2) * 2 / 1 * 0.29'
+ pd='2*int((1 + 1)/2) * (2 / 1 + 0.29)' ps='2*int((1 + 2)/2) * (2 / 1 + 0.29)' nrd='0.29 / 2 ' nrs='0.29 / 2 '
+ sa=0 sb=0 sd=0 mult=1 m=1
xinv x VGND VGND VDPWR VDPWR cmp_raw sky130_fd_sc_hd__inv_1
.ends

.end
